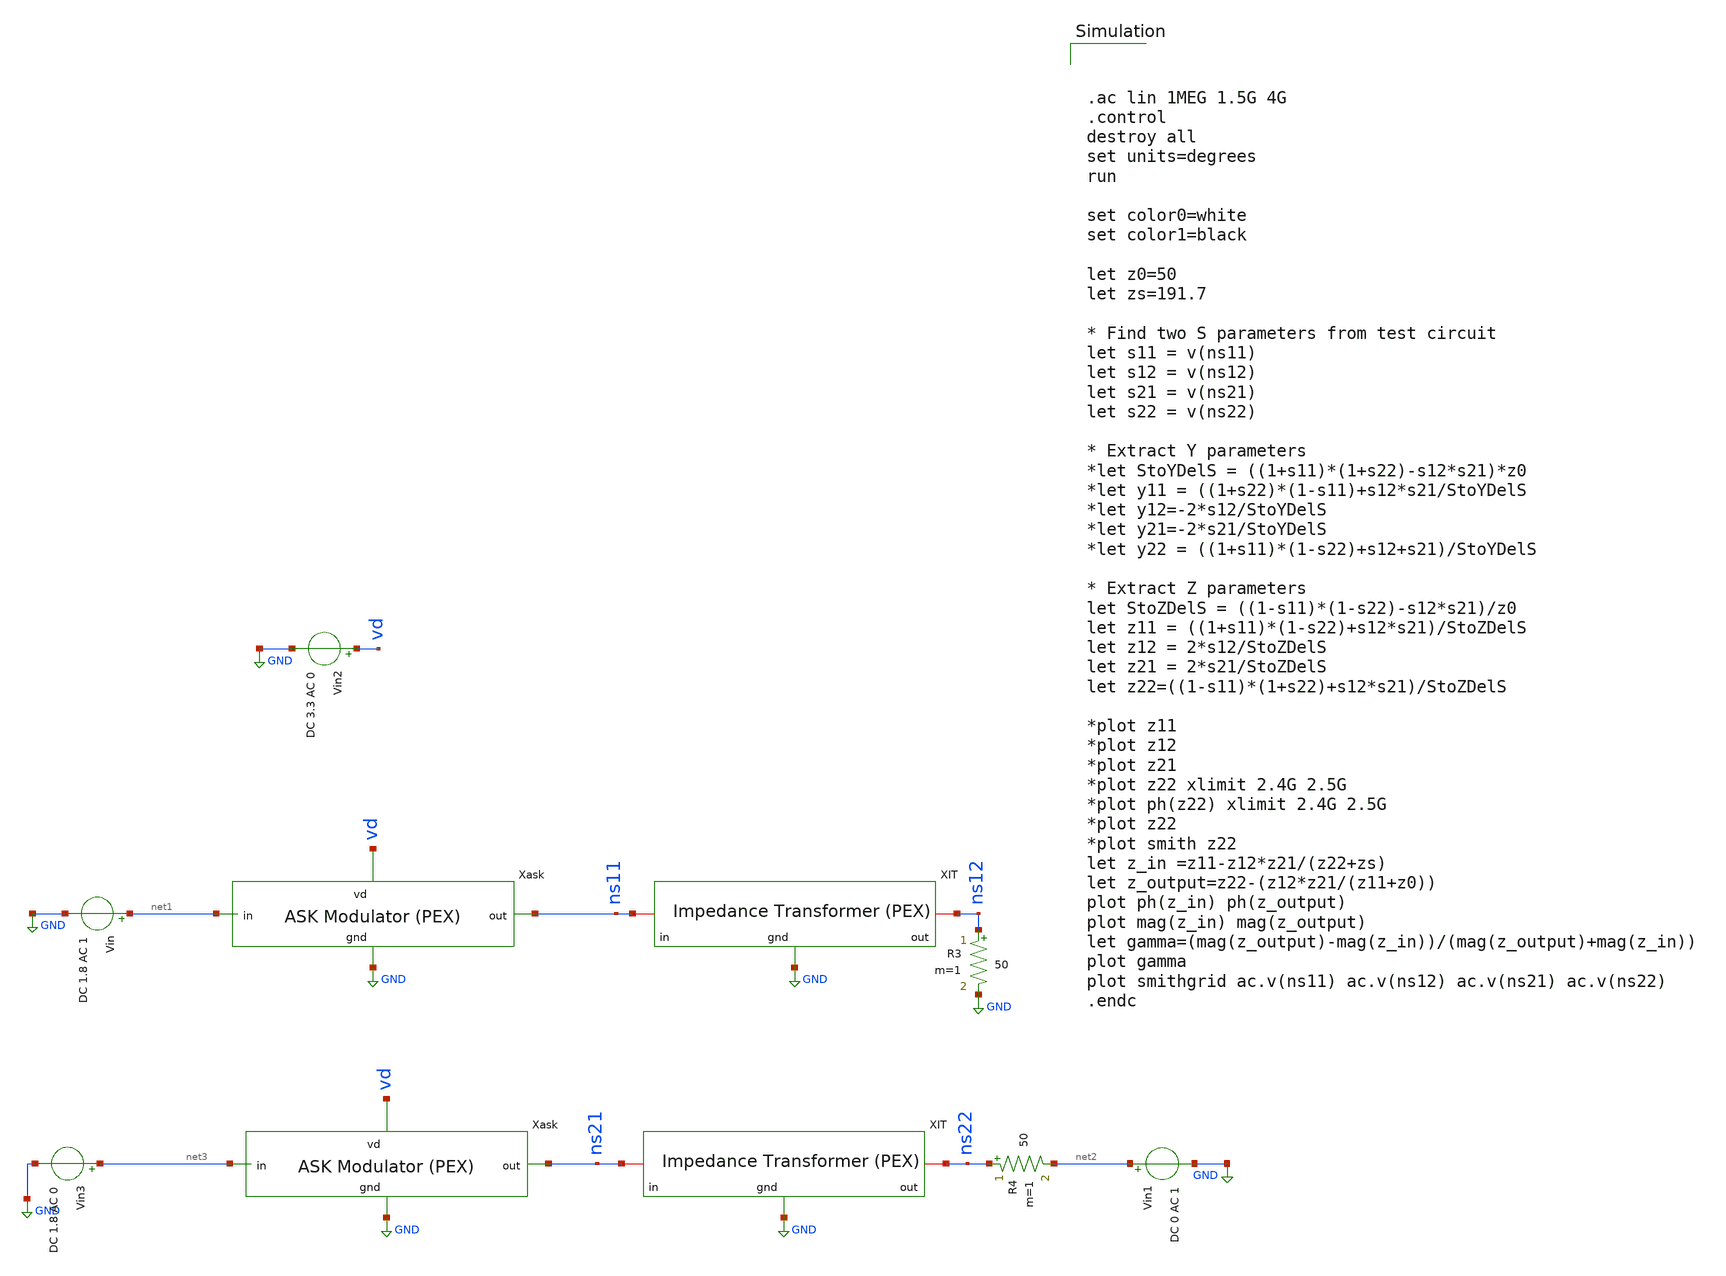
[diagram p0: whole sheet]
** sch_path: impedance-transformer/xschem/impedance-transformer-pex_tb-ac.sch
**.subckt impedance-transformer-pex_tb-ac
Vin net1 GND DC 1.8 AC 1
Vin1 net2 GND DC 0 AC 1
R3 ns12 GND 50 m=1
R4 ns22 net2 50 m=1
xit1 ns11 ns12 GND impedance-transformer-pex
xit2 ns21 ns22 GND impedance-transformer-pex
x1 vd ns11 net1 GND ask-modulator-pex
x2 vd ns21 net3 GND ask-modulator-pex
Vin2 vd GND DC 3.3 AC 0
Vin3 net3 GND DC 1.8 AC 0
**** begin user architecture code



.ac lin 1MEG 1.5G 4G
.control
destroy all
set units=degrees
run

set color0=white
set color1=black

let z0=50
let zs=191.7

* Find two S parameters from test circuit
let s11 = v(ns11)
let s12 = v(ns12)
let s21 = v(ns21)
let s22 = v(ns22)

* Extract Y parameters
*let StoYDelS = ((1+s11)*(1+s22)-s12*s21)*z0
*let y11 = ((1+s22)*(1-s11)+s12*s21/StoYDelS
*let y12=-2*s12/StoYDelS
*let y21=-2*s21/StoYDelS
*let y22 = ((1+s11)*(1-s22)+s12+s21)/StoYDelS

* Extract Z parameters
let StoZDelS = ((1-s11)*(1-s22)-s12*s21)/z0
let z11 = ((1+s11)*(1-s22)+s12*s21)/StoZDelS
let z12 = 2*s12/StoZDelS
let z21 = 2*s21/StoZDelS
let z22=((1-s11)*(1+s22)+s12*s21)/StoZDelS

*plot z11
*plot z12
*plot z21
*plot z22 xlimit 2.4G 2.5G
*plot ph(z22) xlimit 2.4G 2.5G
*plot z22
*plot smith z22
let z_in =z11-z12*z21/(z22+zs)
let z_output=z22-(z12*z21/(z11+z0))
plot ph(z_in) ph(z_output)
plot mag(z_in) mag(z_output)
let gamma=(mag(z_output)-mag(z_in))/(mag(z_output)+mag(z_in))
plot gamma
plot smithgrid ac.v(ns11) ac.v(ns12) ac.v(ns21) ac.v(ns22)
.endc


.lib /home/hugodg/sky130_workspace/skywater-pdk/libraries/sky130_fd_pr_ngspice/latest/models/sky130.lib.spice tt

**** end user architecture code
**.ends
.GLOBAL GND
.end
